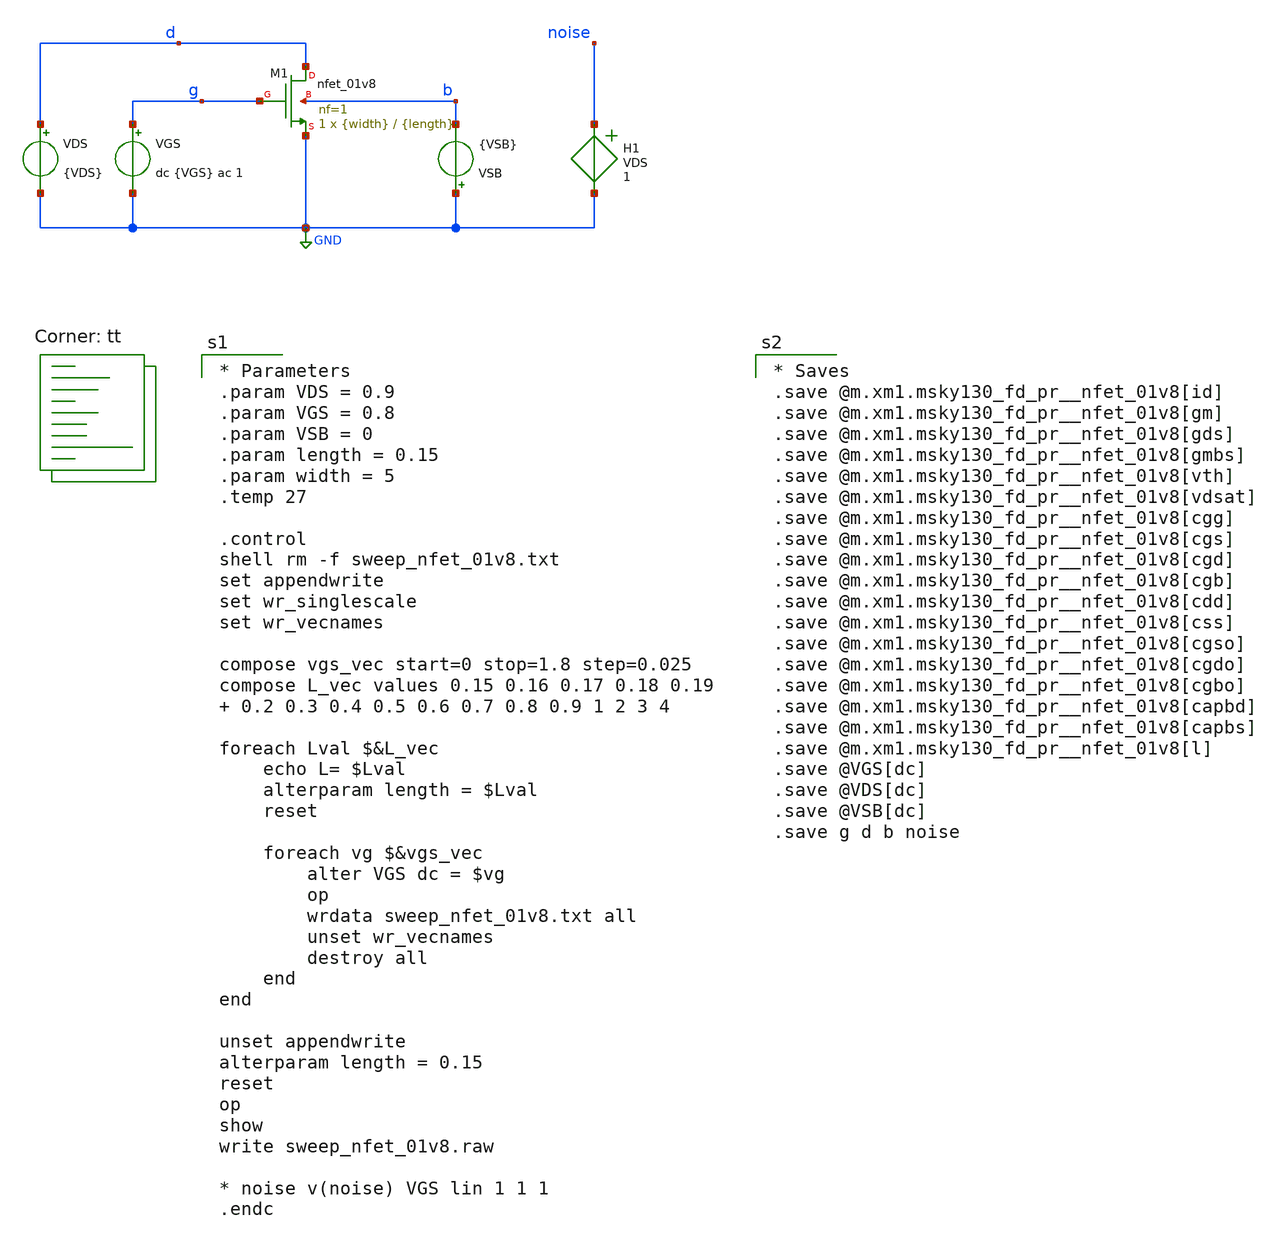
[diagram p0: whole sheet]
** sch_path: analog/gm-ID-LUT/schematics/sweep_nfet_01v8.sch
**.subckt sweep_nfet_01v8
XM1 d g GND b sky130_fd_pr__nfet_01v8 L={length} W={width} nf=1 ad='int((nf+1)/2) * W/nf * 0.29' as='int((nf+2)/2) * W/nf * 0.29'
+ pd='2*int((nf+1)/2) * (W/nf + 0.29)' ps='2*int((nf+2)/2) * (W/nf + 0.29)' nrd='0.29 / W' nrs='0.29 / W'
+ sa=0 sb=0 sd=0 mult=1 m=1
VDS d GND {VDS}
VGS g GND dc {VGS} ac 1
VSB GND b {VSB}
H1 noise GND VDS 1
**** begin user architecture code
.lib $::SKYWATER_MODELS/sky130.lib.spice tt

* Parameters
.param VDS = 0.9
.param VGS = 0.8
.param VSB = 0
.param length = 0.15
.param width = 5
.temp 27

.control
shell rm -f sweep_nfet_01v8.txt
set appendwrite
set wr_singlescale
set wr_vecnames

compose vgs_vec start=0 stop=1.8 step=0.025
compose L_vec values 0.15 0.16 0.17 0.18 0.19  0.2 0.3 0.4 0.5 0.6 0.7 0.8 0.9 1 2 3 4

foreach Lval $&L_vec
    echo L= $Lval
    alterparam length = $Lval
    reset

    foreach vg $&vgs_vec
        alter VGS dc = $vg
        op
        wrdata sweep_nfet_01v8.txt all
        unset wr_vecnames
        destroy all
    end
end

unset appendwrite
alterparam length = 0.15
reset
op
show
write sweep_nfet_01v8.raw

* noise v(noise) VGS lin 1 1 1
.endc



* Saves
.save @m.xm1.msky130_fd_pr__nfet_01v8[id]
.save @m.xm1.msky130_fd_pr__nfet_01v8[gm]
.save @m.xm1.msky130_fd_pr__nfet_01v8[gds]
.save @m.xm1.msky130_fd_pr__nfet_01v8[gmbs]
.save @m.xm1.msky130_fd_pr__nfet_01v8[vth]
.save @m.xm1.msky130_fd_pr__nfet_01v8[vdsat]
.save @m.xm1.msky130_fd_pr__nfet_01v8[cgg]
.save @m.xm1.msky130_fd_pr__nfet_01v8[cgs]
.save @m.xm1.msky130_fd_pr__nfet_01v8[cgd]
.save @m.xm1.msky130_fd_pr__nfet_01v8[cgb]
.save @m.xm1.msky130_fd_pr__nfet_01v8[cdd]
.save @m.xm1.msky130_fd_pr__nfet_01v8[css]
.save @m.xm1.msky130_fd_pr__nfet_01v8[cgso]
.save @m.xm1.msky130_fd_pr__nfet_01v8[cgdo]
.save @m.xm1.msky130_fd_pr__nfet_01v8[cgbo]
.save @m.xm1.msky130_fd_pr__nfet_01v8[capbd]
.save @m.xm1.msky130_fd_pr__nfet_01v8[capbs]
.save @m.xm1.msky130_fd_pr__nfet_01v8[l]
.save @VGS[dc]
.save @VDS[dc]
.save @VSB[dc]
.save g d b noise


**** end user architecture code
**.ends
.GLOBAL GND
.end
